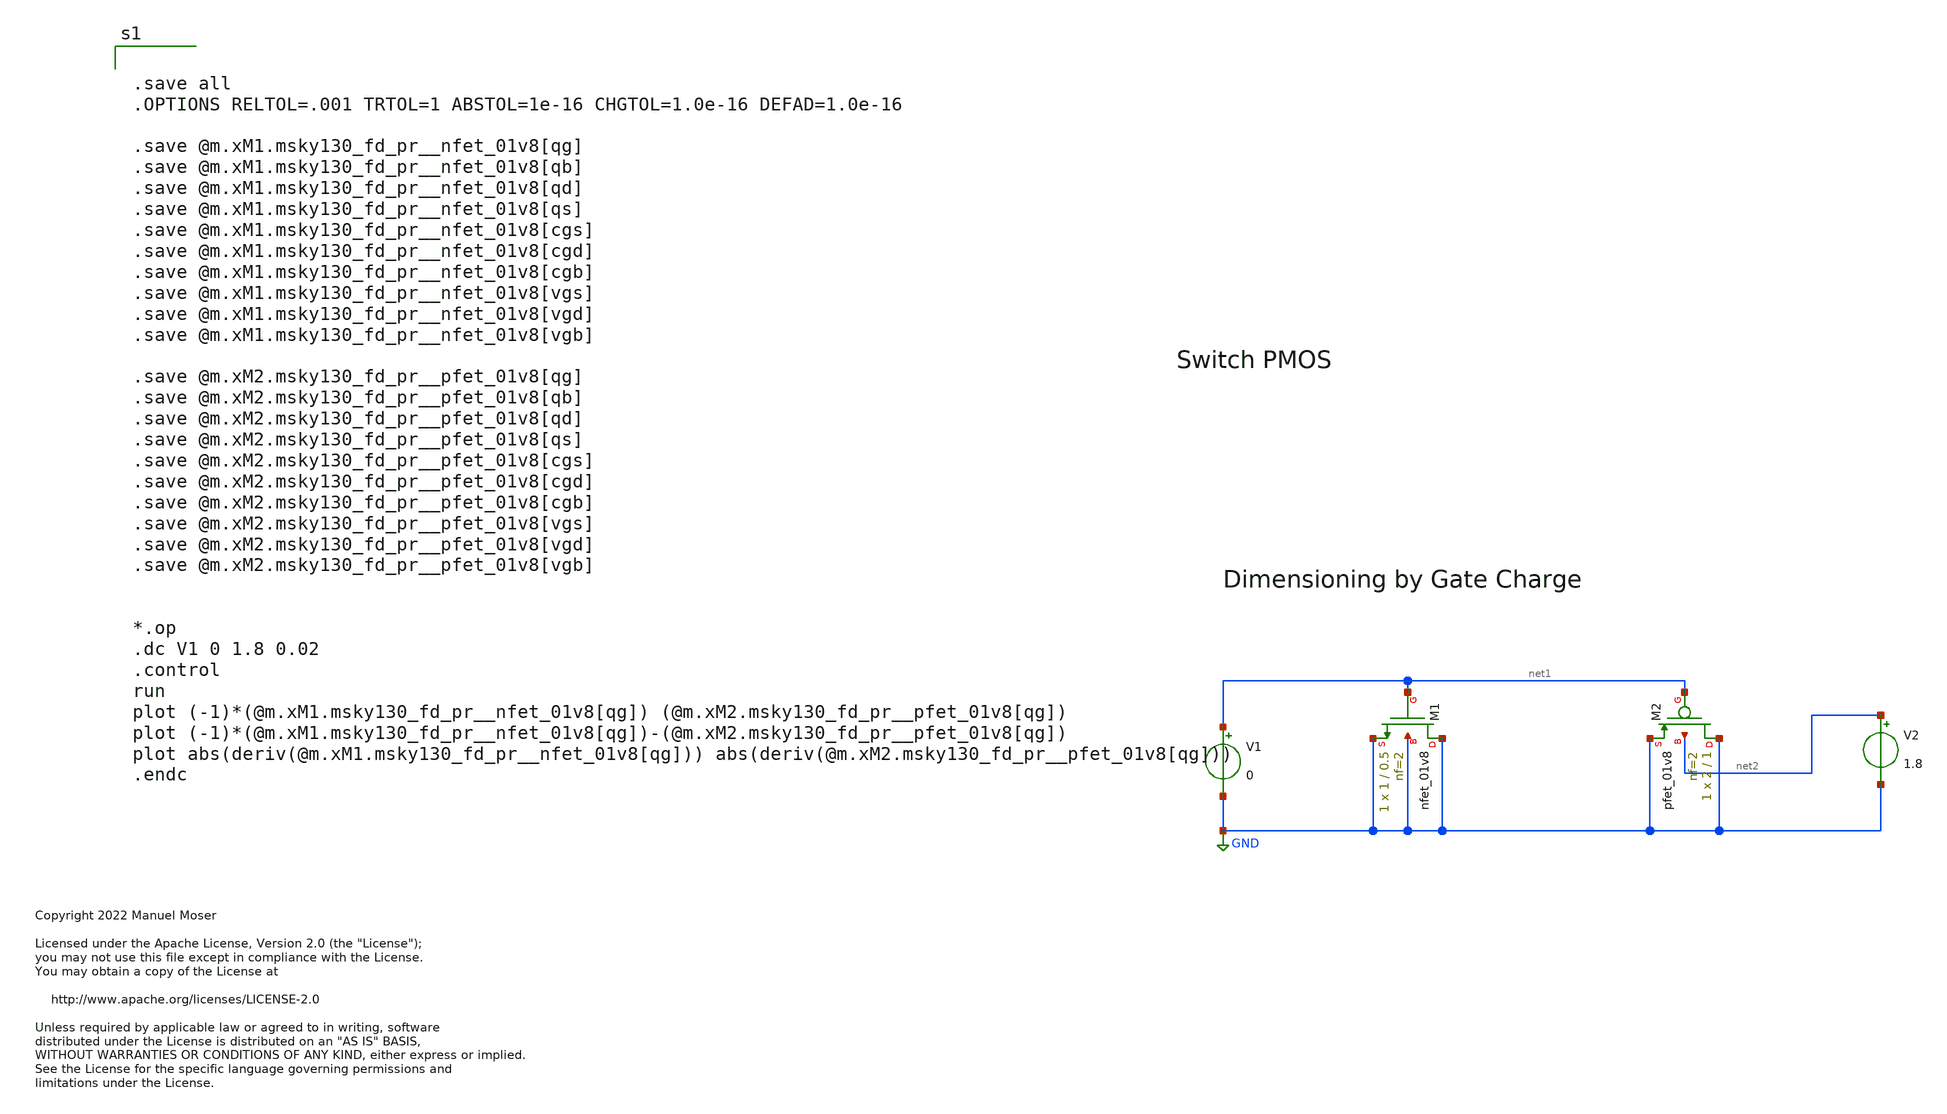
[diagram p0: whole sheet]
** sch_path: xschem/adc_array_circuit_gate_sizing.sch
* Copyright 2022 Manuel Moser
* Licensed under the Apache License, Version 2.0 (the "License");
**.subckt adc_array_circuit_gate_sizing
XM1 GND net1 GND GND sky130_fd_pr__nfet_01v8 L=0.5 W=1 nf=2 ad='int((nf+1)/2) * W/nf * 0.29' as='int((nf+2)/2) * W/nf * 0.29'
+ pd='2*int((nf+1)/2) * (W/nf + 0.29)' ps='2*int((nf+2)/2) * (W/nf + 0.29)' nrd='0.29 / W' nrs='0.29 / W'
+ sa=0 sb=0 sd=0 mult=1 m=1
XM2 GND net1 GND net2 sky130_fd_pr__pfet_01v8 L=1 W=2 nf=2 ad='int((nf+1)/2) * W/nf * 0.29' as='int((nf+2)/2) * W/nf * 0.29'
+ pd='2*int((nf+1)/2) * (W/nf + 0.29)' ps='2*int((nf+2)/2) * (W/nf + 0.29)' nrd='0.29 / W' nrs='0.29 / W'
+ sa=0 sb=0 sd=0 mult=1 m=1
V1 net1 GND 0
V2 net2 GND 1.8
**** begin user architecture code


.save all
.OPTIONS RELTOL=.001 TRTOL=1 ABSTOL=1e-16 CHGTOL=1.0e-16 DEFAD=1.0e-16

.save @m.xM1.msky130_fd_pr__nfet_01v8[qg]
.save @m.xM1.msky130_fd_pr__nfet_01v8[qb]
.save @m.xM1.msky130_fd_pr__nfet_01v8[qd]
.save @m.xM1.msky130_fd_pr__nfet_01v8[qs]
.save @m.xM1.msky130_fd_pr__nfet_01v8[cgs]
.save @m.xM1.msky130_fd_pr__nfet_01v8[cgd]
.save @m.xM1.msky130_fd_pr__nfet_01v8[cgb]
.save @m.xM1.msky130_fd_pr__nfet_01v8[vgs]
.save @m.xM1.msky130_fd_pr__nfet_01v8[vgd]
.save @m.xM1.msky130_fd_pr__nfet_01v8[vgb]

.save @m.xM2.msky130_fd_pr__pfet_01v8[qg]
.save @m.xM2.msky130_fd_pr__pfet_01v8[qb]
.save @m.xM2.msky130_fd_pr__pfet_01v8[qd]
.save @m.xM2.msky130_fd_pr__pfet_01v8[qs]
.save @m.xM2.msky130_fd_pr__pfet_01v8[cgs]
.save @m.xM2.msky130_fd_pr__pfet_01v8[cgd]
.save @m.xM2.msky130_fd_pr__pfet_01v8[cgb]
.save @m.xM2.msky130_fd_pr__pfet_01v8[vgs]
.save @m.xM2.msky130_fd_pr__pfet_01v8[vgd]
.save @m.xM2.msky130_fd_pr__pfet_01v8[vgb]


*.op
.dc V1 0 1.8 0.02
.control
run
plot (-1)*(@m.xM1.msky130_fd_pr__nfet_01v8[qg]) (@m.xM2.msky130_fd_pr__pfet_01v8[qg])
plot (-1)*(@m.xM1.msky130_fd_pr__nfet_01v8[qg])-(@m.xM2.msky130_fd_pr__pfet_01v8[qg])
plot abs(deriv(@m.xM1.msky130_fd_pr__nfet_01v8[qg])) abs(deriv(@m.xM2.msky130_fd_pr__pfet_01v8[qg]))
.endc



.lib $::SKYWATER_MODELS/sky130.lib.spice tt
**** end user architecture code
**.ends
.GLOBAL GND
.end
